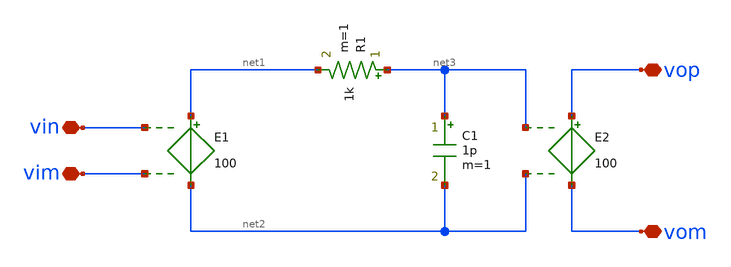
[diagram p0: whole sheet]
** sch_path: xschem/untitled-3.sch
**.subckt untitled-3 vim vin vop vom
*.iopin vim
*.iopin vin
*.iopin vop
*.iopin vom
E1 net1 net2 vin vim 100
R1 net3 net1 1k m=1
C1 net3 net2 1p m=1
E2 vop vom net3 net2 100
**.ends
.end
